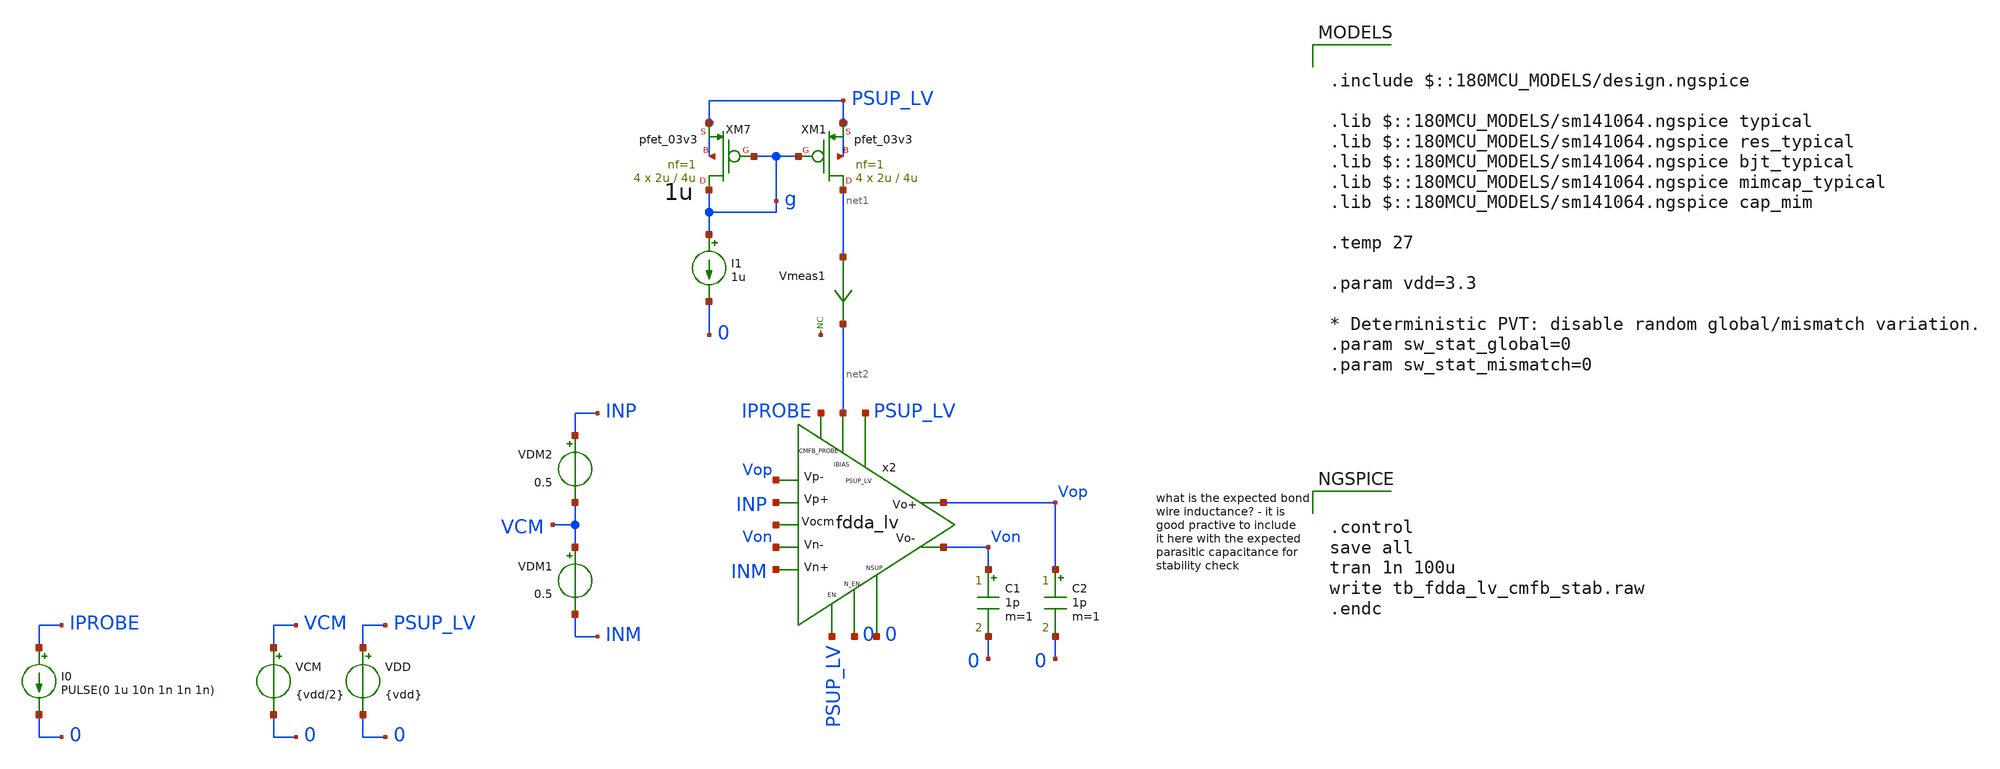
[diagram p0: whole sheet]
** sch_path: xschem/blocks/fdda_lv/tb_fdda_lv_cmfb_stab.sch
**.subckt tb_fdda_lv_cmfb_stab
C1 Von 0 1p m=1
x2 PSUP_LV Vop Von INM INP Vop Von net2 0 PSUP_LV 0 IPROBE net3 fdda_lv
VDD PSUP_LV 0 {vdd}
C2 Vop 0 1p m=1
VCM VCM 0 {vdd/2}
VDM2 INP VCM 0.5
VDM1 VCM INM 0.5
I0 IPROBE 0 PULSE(0 1u 10n 1n 1n 1n)
* noconn #net4
XM7 g g PSUP_LV PSUP_LV pfet_03v3 L=4u W=2u nf=1 ad='int((nf+1)/2) * W/nf * 0.18u' as='int((nf+2)/2) * W/nf * 0.18u'
+ pd='2*int((nf+1)/2) * (W/nf + 0.18u)' ps='2*int((nf+2)/2) * (W/nf + 0.18u)' nrd='0.18u / W' nrs='0.18u / W'
+ sa=0 sb=0 sd=0 m=4
XM1 net1 g PSUP_LV PSUP_LV pfet_03v3 L=4u W=2u nf=1 ad='int((nf+1)/2) * W/nf * 0.18u' as='int((nf+2)/2) * W/nf * 0.18u'
+ pd='2*int((nf+1)/2) * (W/nf + 0.18u)' ps='2*int((nf+2)/2) * (W/nf + 0.18u)' nrd='0.18u / W' nrs='0.18u / W'
+ sa=0 sb=0 sd=0 m=4
I1 g 0 1u
Vmeas1 net1 net2 0
.save i(vmeas1)
**** begin user architecture code

.include $::180MCU_MODELS/design.ngspice

.lib $::180MCU_MODELS/sm141064.ngspice typical
.lib $::180MCU_MODELS/sm141064.ngspice res_typical
.lib $::180MCU_MODELS/sm141064.ngspice bjt_typical
.lib $::180MCU_MODELS/sm141064.ngspice mimcap_typical
.lib $::180MCU_MODELS/sm141064.ngspice cap_mim

.temp 27

.param vdd=3.3

* Deterministic PVT: disable random global/mismatch variation.
.param sw_stat_global=0
.param sw_stat_mismatch=0



.control
save all
tran 1n 100u
write tb_fdda_lv_cmfb_stab.raw
.endc


**** end user architecture code
**.ends
.end
